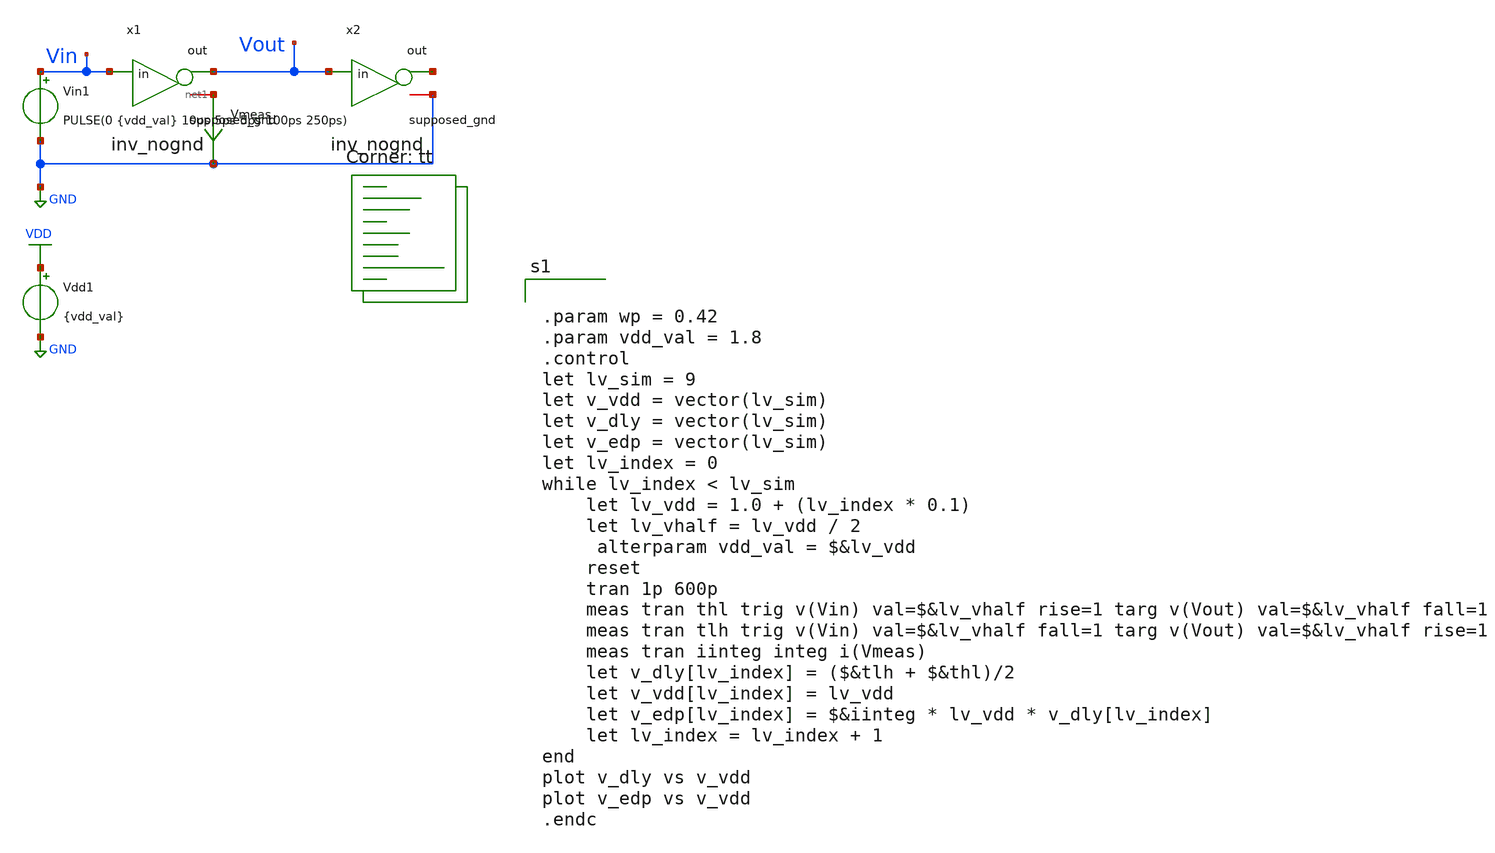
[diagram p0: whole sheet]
** sch_path: tut3/expt1_b/expt1_b.sch
**.subckt expt1_b
x1 Vout Vin net1 inv_nognd
x2 net2 Vout GND inv_nognd
Vin1 Vin GND PULSE(0 {vdd_val} 10ps 5ps 5ps 100ps 250ps)
Vdd1 VDD GND {vdd_val}
Vmeas net1 GND 0
**** begin user architecture code
.lib $::SKYWATER_MODELS/sky130.lib.spice tt


.param wp = 0.42
.param vdd_val = 1.8
.control
let lv_sim = 9
let v_vdd = vector(lv_sim)
let v_dly = vector(lv_sim)
let v_edp = vector(lv_sim)
let lv_index = 0
while lv_index < lv_sim
	let lv_vdd = 1.0 + (lv_index * 0.1)
	let lv_vhalf = lv_vdd / 2
 	alterparam vdd_val = $&lv_vdd
	reset
	tran 1p 600p
	meas tran thl trig v(Vin) val=$&lv_vhalf rise=1 targ v(Vout) val=$&lv_vhalf fall=1
	meas tran tlh trig v(Vin) val=$&lv_vhalf fall=1 targ v(Vout) val=$&lv_vhalf rise=1
	meas tran iinteg integ i(Vmeas)
	let v_dly[lv_index] = ($&tlh + $&thl)/2
	let v_vdd[lv_index] = lv_vdd
	let v_edp[lv_index] = $&iinteg * lv_vdd * v_dly[lv_index]
	let lv_index = lv_index + 1
end
plot v_dly vs v_vdd
plot v_edp vs v_vdd
.endc


**** end user architecture code
**.ends
.GLOBAL GND
.GLOBAL VDD
.end
